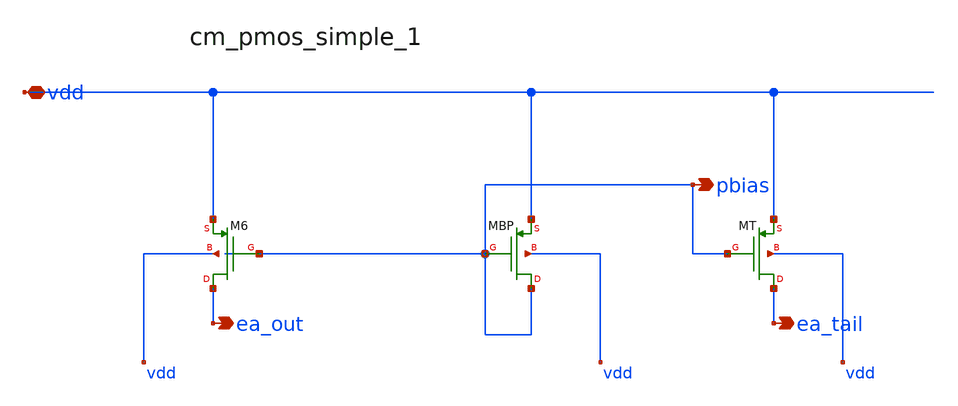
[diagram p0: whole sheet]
** sch_path: analog-db/raw/ldo_010_capless_lowiq/hier/blocks/cm_pmos_simple_1.sch
**.subckt cm_pmos_simple_1 vdd pbias ea_out ea_tail
*.iopin vdd
*.opin pbias
*.opin ea_out
*.opin ea_tail
XM6 ea_out pbias vdd vdd sg13_lv_pmos w=x_dut_xm6_w l=x_dut_xmbp_l ng=1 m=1
XMBP pbias pbias vdd vdd sg13_lv_pmos w=x_dut_xmbp_w l=x_dut_xmbp_l ng=1 m=1
XMT ea_tail pbias vdd vdd sg13_lv_pmos w=x_dut_xmt_w l=x_dut_xmbp_l ng=1 m=1
**.ends
.end
